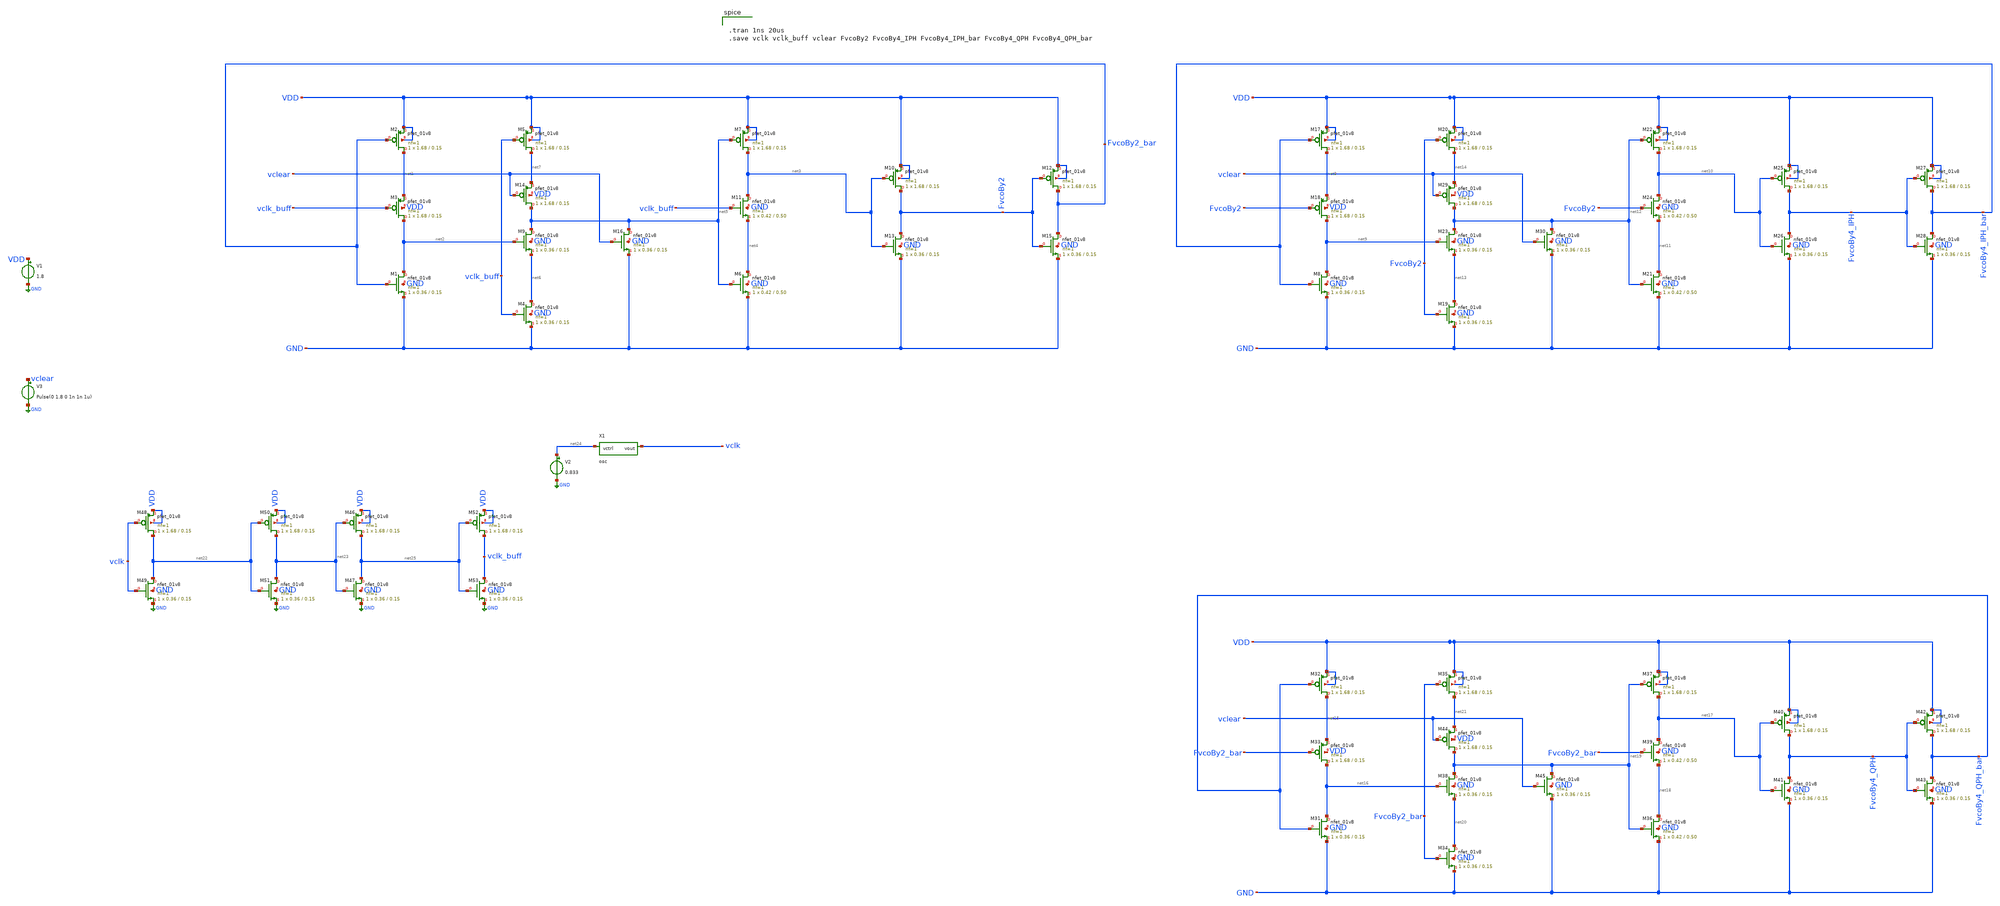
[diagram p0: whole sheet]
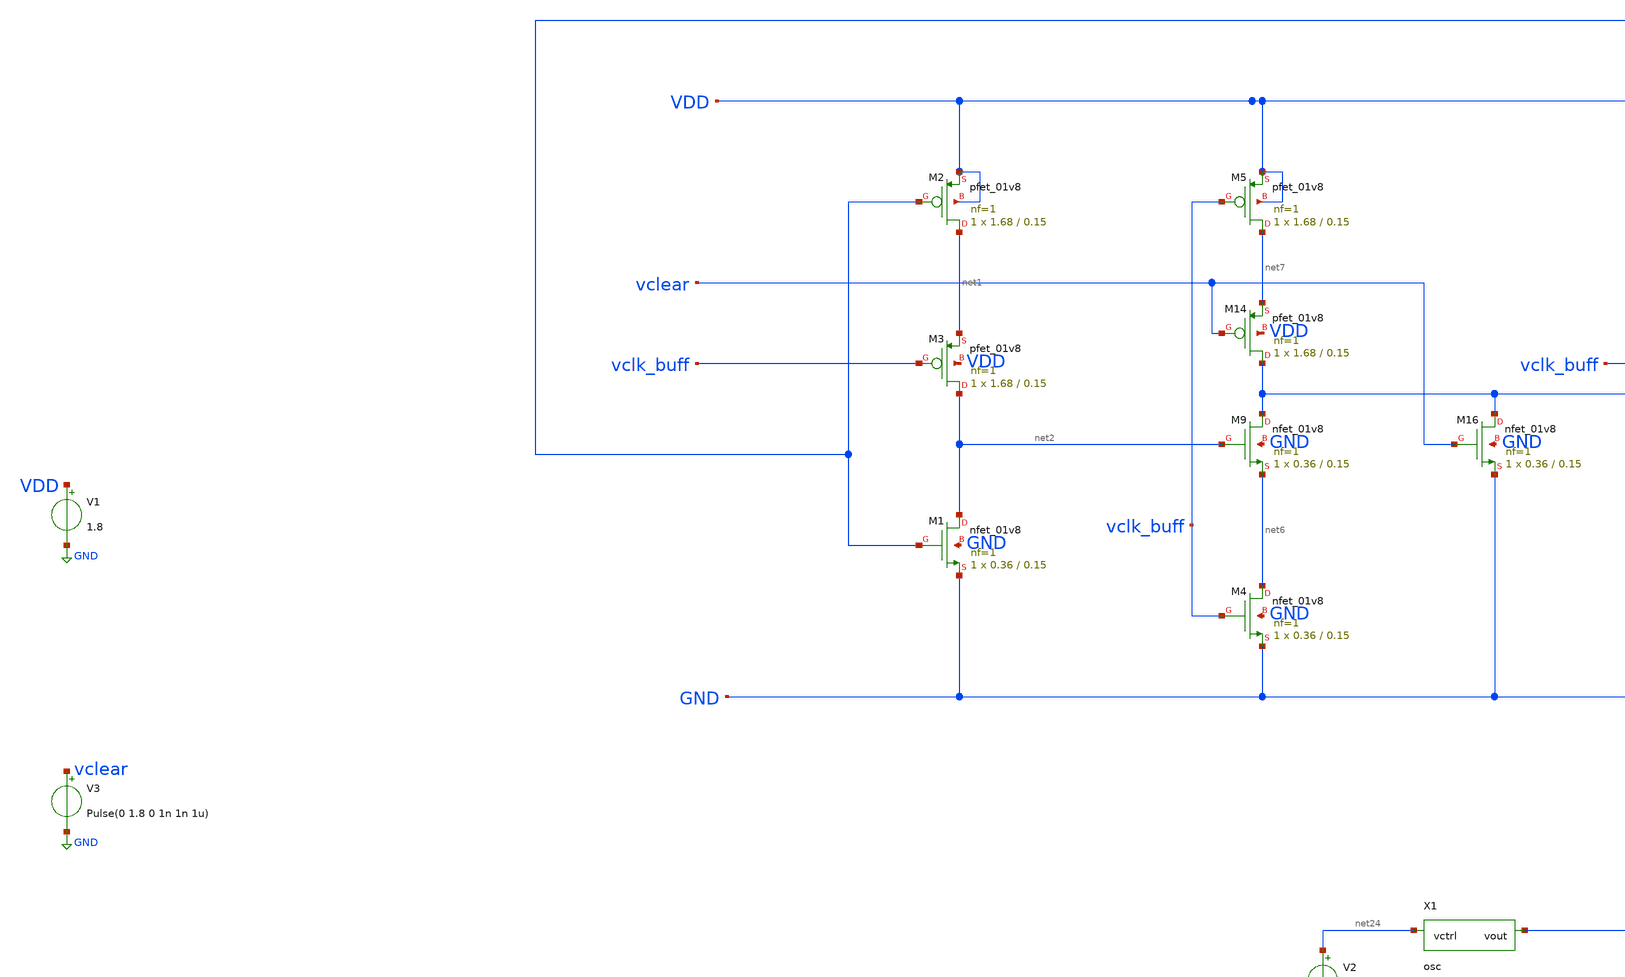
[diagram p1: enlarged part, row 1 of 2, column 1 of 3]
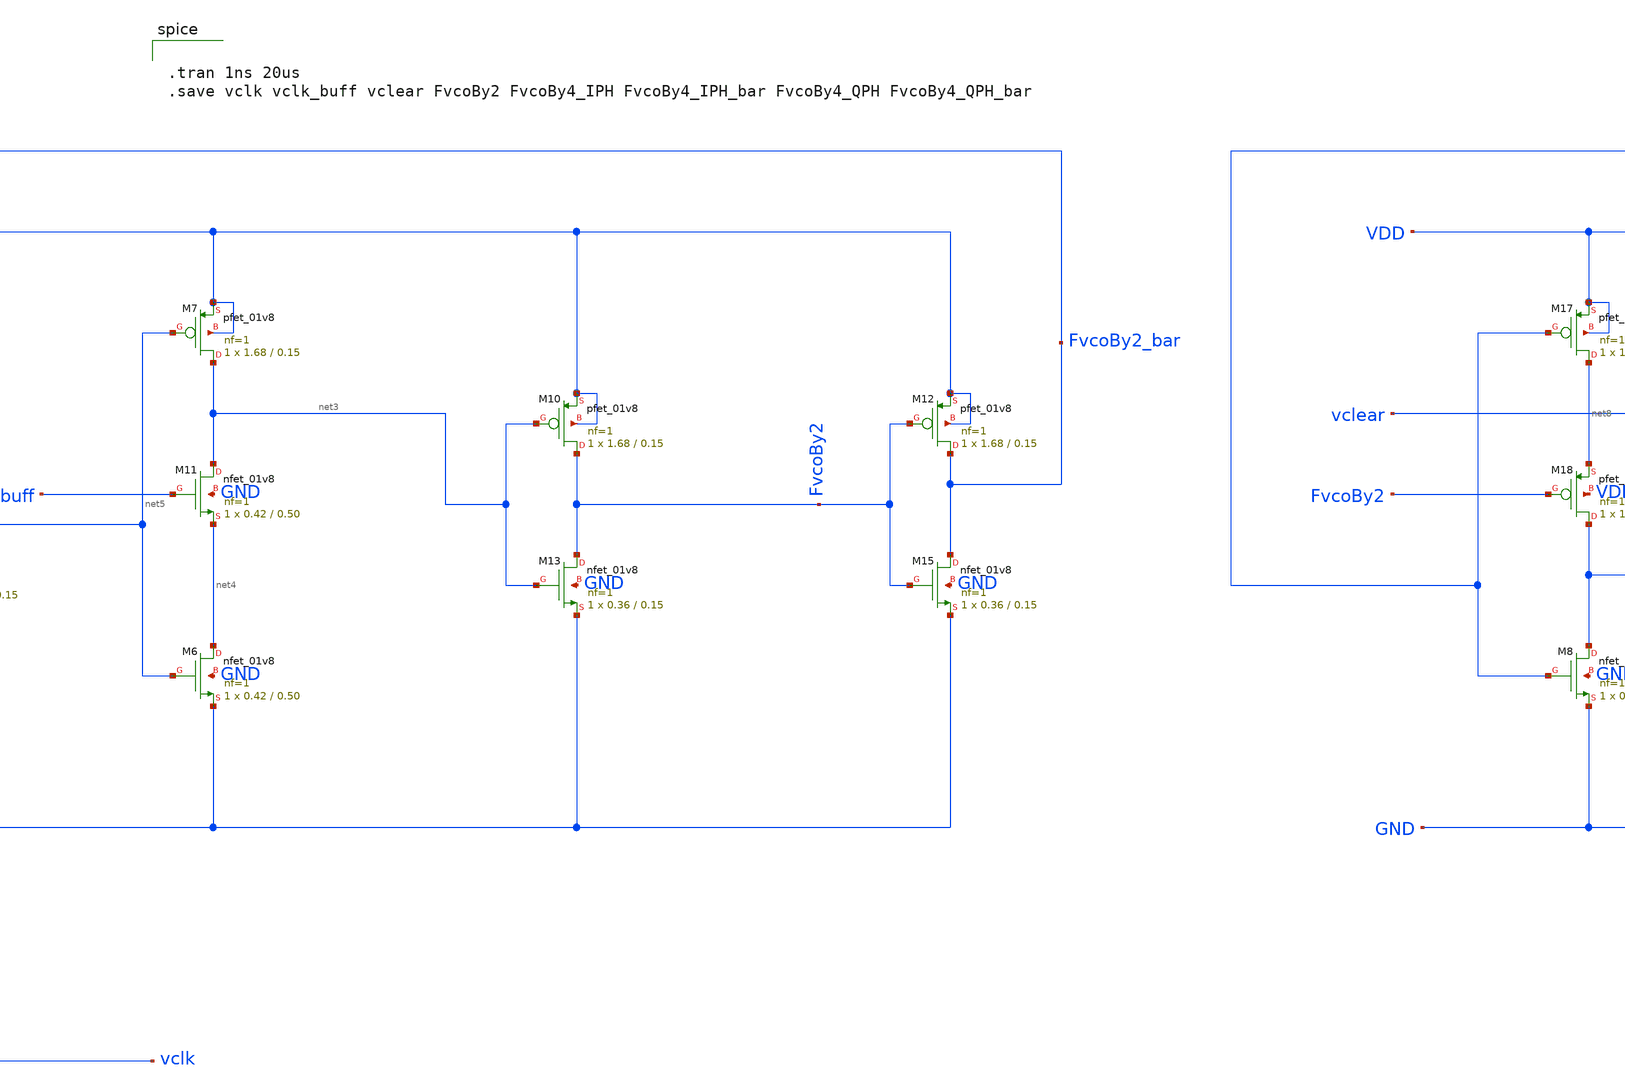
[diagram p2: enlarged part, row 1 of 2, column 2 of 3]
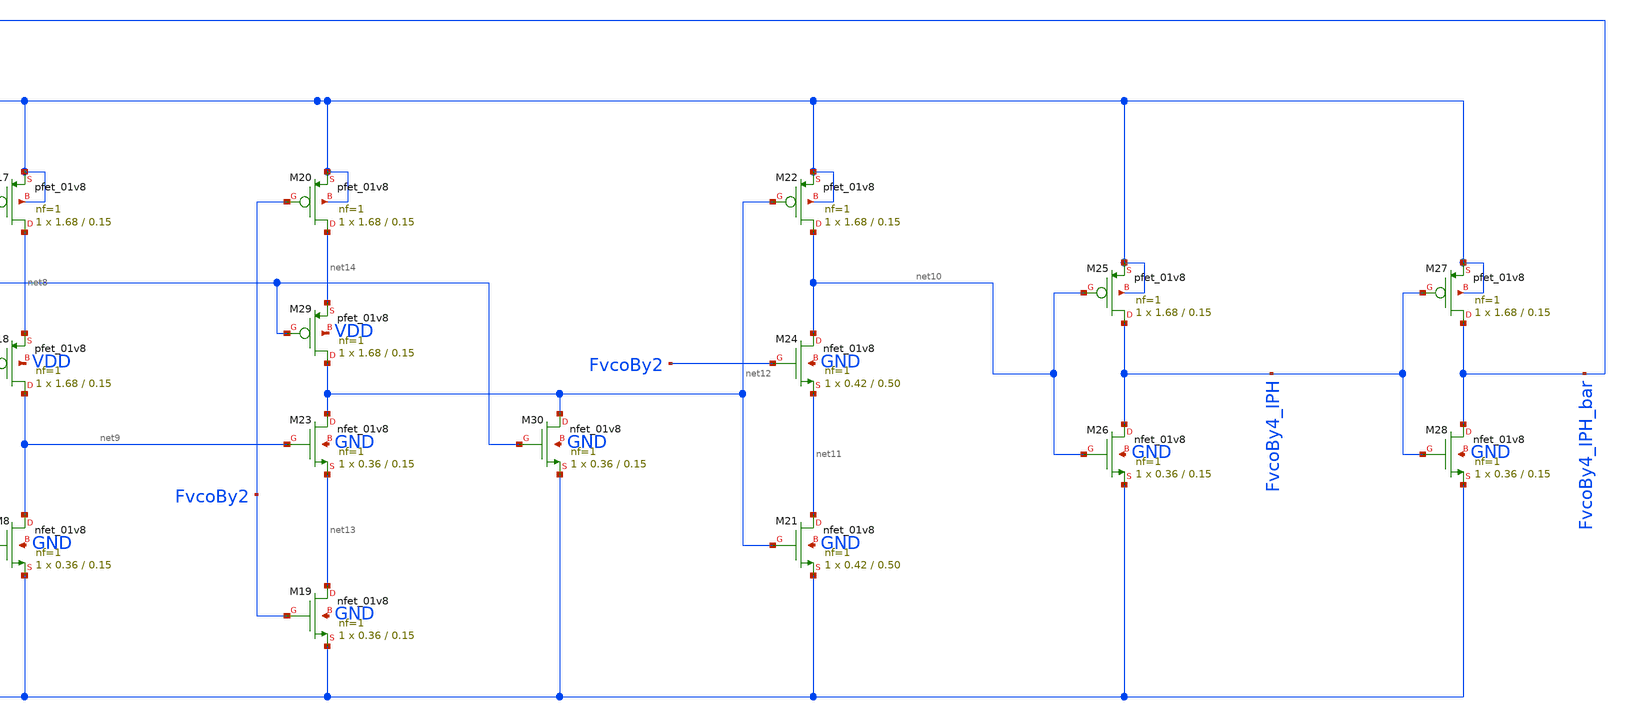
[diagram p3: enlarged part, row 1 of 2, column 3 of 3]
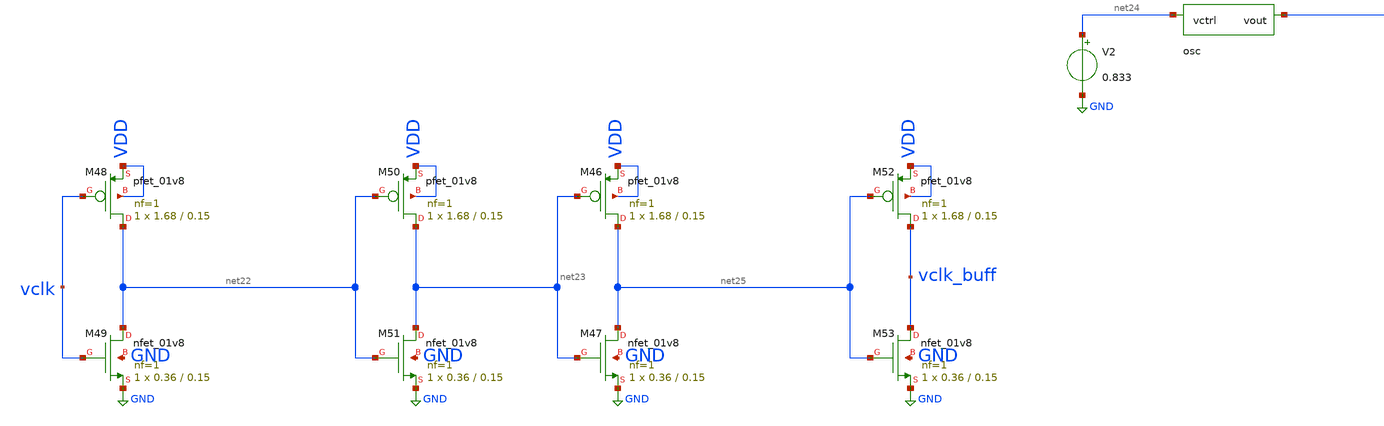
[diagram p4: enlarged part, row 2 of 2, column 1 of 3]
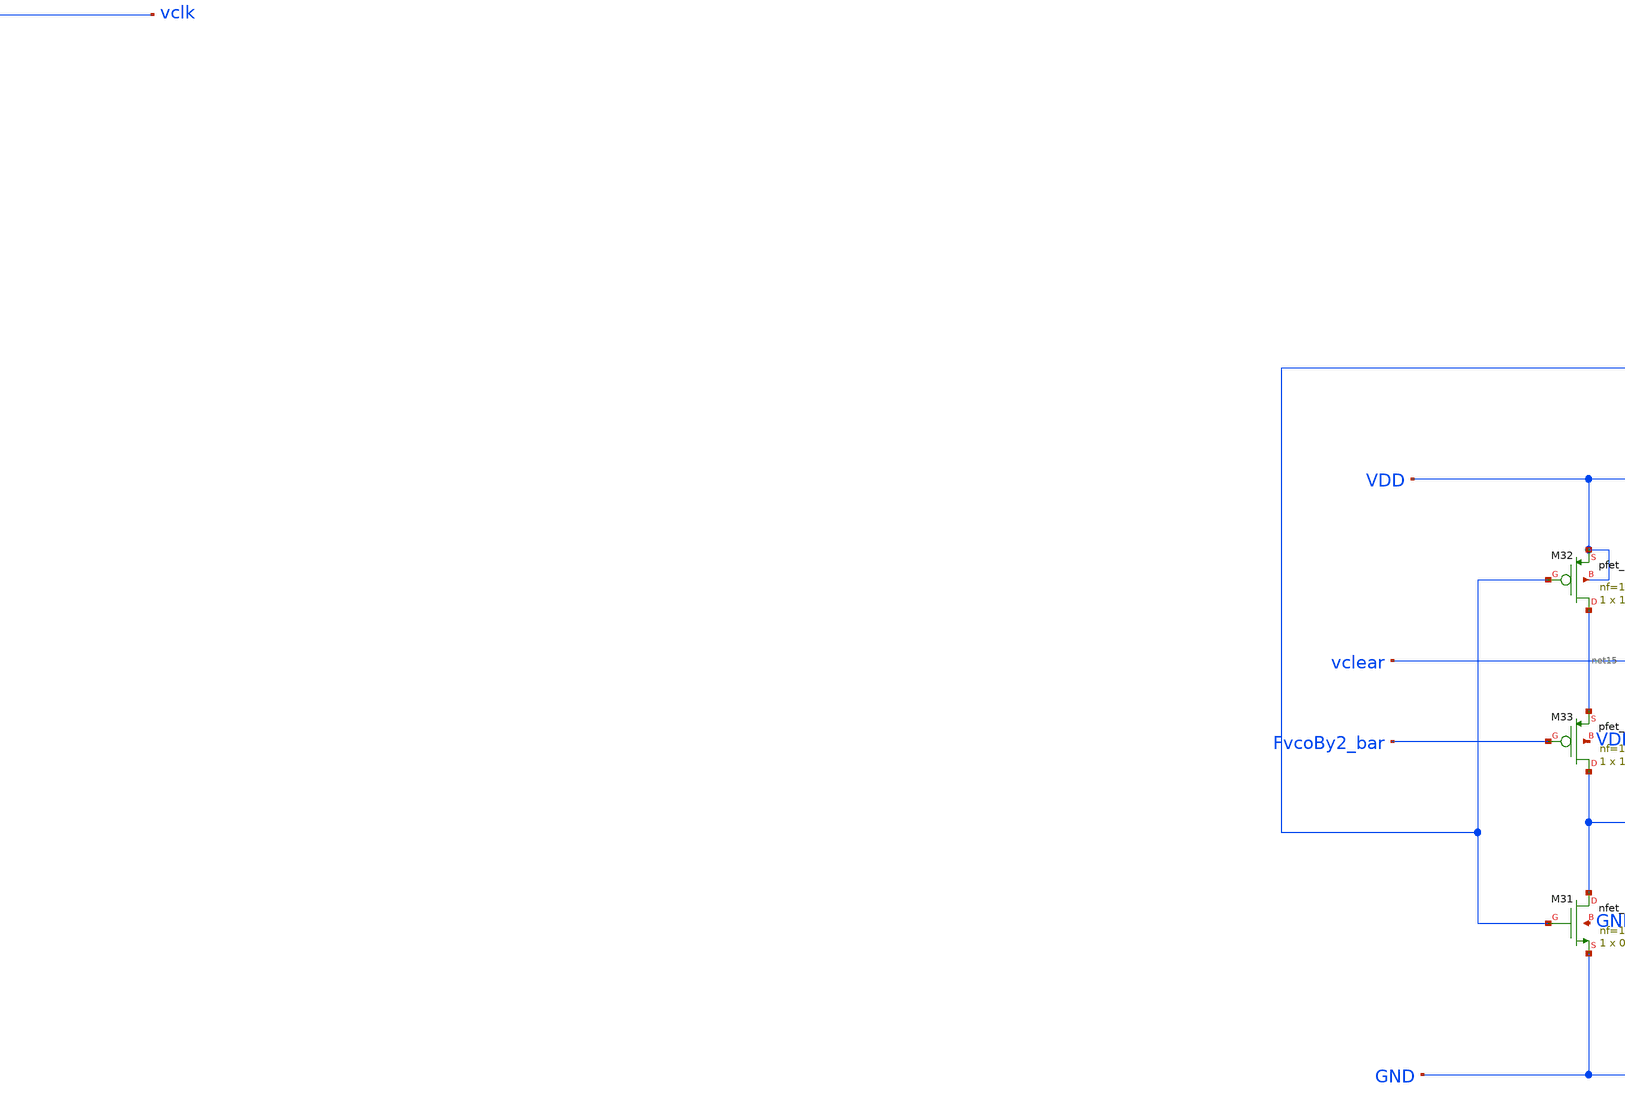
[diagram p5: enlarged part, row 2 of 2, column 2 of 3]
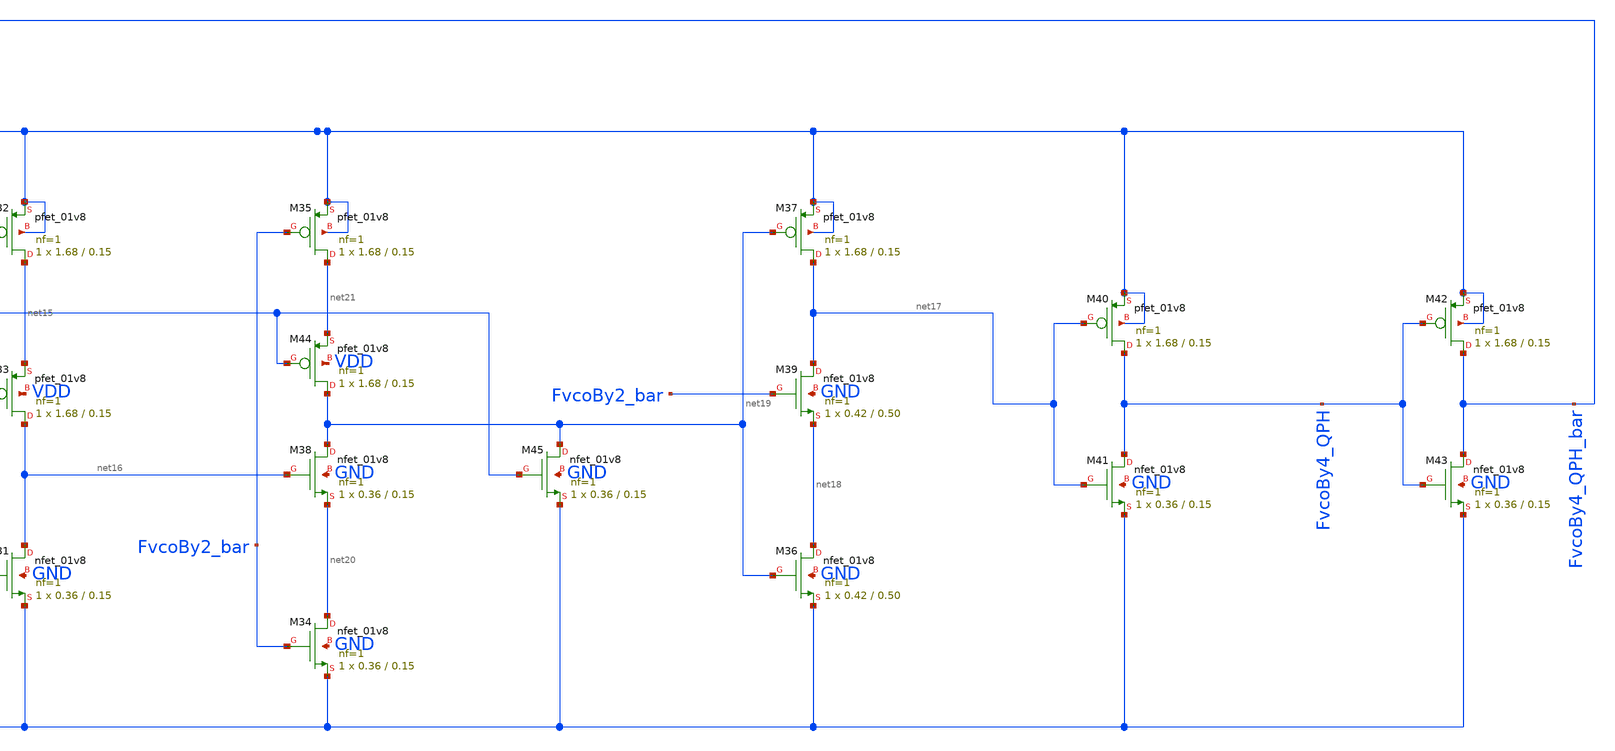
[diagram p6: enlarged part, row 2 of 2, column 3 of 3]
** sch_path: freqBy4_instant.sch
**.subckt freqBy4_instant
XM1 net2 FvcoBy2_bar GND GND sky130_fd_pr__nfet_01v8 L=0.15 W=0.36 nf=1 ad='int((nf+1)/2) * W/nf * 0.29'
+ as='int((nf+2)/2) * W/nf * 0.29' pd='2*int((nf+1)/2) * (W/nf + 0.29)' ps='2*int((nf+2)/2) * (W/nf + 0.29)'
+ nrd='0.29 / W' nrs='0.29 / W' sa=0 sb=0 sd=0 mult=1 m=1
XM2 net1 FvcoBy2_bar VDD VDD sky130_fd_pr__pfet_01v8 L=0.15 W=1.68 nf=1 ad='int((nf+1)/2) * W/nf * 0.29'
+ as='int((nf+2)/2) * W/nf * 0.29' pd='2*int((nf+1)/2) * (W/nf + 0.29)' ps='2*int((nf+2)/2) * (W/nf + 0.29)'
+ nrd='0.29 / W' nrs='0.29 / W' sa=0 sb=0 sd=0 mult=1 m=1
XM3 net2 vclk_buff net1 VDD sky130_fd_pr__pfet_01v8 L=0.15 W=1.68 nf=1 ad='int((nf+1)/2) * W/nf * 0.29'
+ as='int((nf+2)/2) * W/nf * 0.29' pd='2*int((nf+1)/2) * (W/nf + 0.29)' ps='2*int((nf+2)/2) * (W/nf + 0.29)'
+ nrd='0.29 / W' nrs='0.29 / W' sa=0 sb=0 sd=0 mult=1 m=1
XM4 net6 vclk_buff GND GND sky130_fd_pr__nfet_01v8 L=0.15 W=0.36 nf=1 ad='int((nf+1)/2) * W/nf * 0.29'
+ as='int((nf+2)/2) * W/nf * 0.29' pd='2*int((nf+1)/2) * (W/nf + 0.29)' ps='2*int((nf+2)/2) * (W/nf + 0.29)'
+ nrd='0.29 / W' nrs='0.29 / W' sa=0 sb=0 sd=0 mult=1 m=1
XM5 net7 vclk_buff VDD VDD sky130_fd_pr__pfet_01v8 L=0.15 W=1.68 nf=1 ad='int((nf+1)/2) * W/nf * 0.29'
+ as='int((nf+2)/2) * W/nf * 0.29' pd='2*int((nf+1)/2) * (W/nf + 0.29)' ps='2*int((nf+2)/2) * (W/nf + 0.29)'
+ nrd='0.29 / W' nrs='0.29 / W' sa=0 sb=0 sd=0 mult=1 m=1
XM6 net4 net5 GND GND sky130_fd_pr__nfet_01v8 L=0.50 W=0.42 nf=1 ad='int((nf+1)/2) * W/nf * 0.29' as='int((nf+2)/2) * W/nf * 0.29'
+ pd='2*int((nf+1)/2) * (W/nf + 0.29)' ps='2*int((nf+2)/2) * (W/nf + 0.29)' nrd='0.29 / W' nrs='0.29 / W'
+ sa=0 sb=0 sd=0 mult=1 m=1
XM7 net3 net5 VDD VDD sky130_fd_pr__pfet_01v8 L=0.15 W=1.68 nf=1 ad='int((nf+1)/2) * W/nf * 0.29' as='int((nf+2)/2) * W/nf * 0.29'
+ pd='2*int((nf+1)/2) * (W/nf + 0.29)' ps='2*int((nf+2)/2) * (W/nf + 0.29)' nrd='0.29 / W' nrs='0.29 / W'
+ sa=0 sb=0 sd=0 mult=1 m=1
XM9 net5 net2 net6 GND sky130_fd_pr__nfet_01v8 L=0.15 W=0.36 nf=1 ad='int((nf+1)/2) * W/nf * 0.29' as='int((nf+2)/2) * W/nf * 0.29'
+ pd='2*int((nf+1)/2) * (W/nf + 0.29)' ps='2*int((nf+2)/2) * (W/nf + 0.29)' nrd='0.29 / W' nrs='0.29 / W'
+ sa=0 sb=0 sd=0 mult=1 m=1
XM11 net3 vclk_buff net4 GND sky130_fd_pr__nfet_01v8 L=0.50 W=0.42 nf=1 ad='int((nf+1)/2) * W/nf * 0.29'
+ as='int((nf+2)/2) * W/nf * 0.29' pd='2*int((nf+1)/2) * (W/nf + 0.29)' ps='2*int((nf+2)/2) * (W/nf + 0.29)'
+ nrd='0.29 / W' nrs='0.29 / W' sa=0 sb=0 sd=0 mult=1 m=1
XM10 FvcoBy2 net3 VDD VDD sky130_fd_pr__pfet_01v8 L=0.15 W=1.68 nf=1 ad='int((nf+1)/2) * W/nf * 0.29'
+ as='int((nf+2)/2) * W/nf * 0.29' pd='2*int((nf+1)/2) * (W/nf + 0.29)' ps='2*int((nf+2)/2) * (W/nf + 0.29)'
+ nrd='0.29 / W' nrs='0.29 / W' sa=0 sb=0 sd=0 mult=1 m=1
XM13 FvcoBy2 net3 GND GND sky130_fd_pr__nfet_01v8 L=0.15 W=0.36 nf=1 ad='int((nf+1)/2) * W/nf * 0.29'
+ as='int((nf+2)/2) * W/nf * 0.29' pd='2*int((nf+1)/2) * (W/nf + 0.29)' ps='2*int((nf+2)/2) * (W/nf + 0.29)'
+ nrd='0.29 / W' nrs='0.29 / W' sa=0 sb=0 sd=0 mult=1 m=1
XM12 FvcoBy2_bar FvcoBy2 VDD VDD sky130_fd_pr__pfet_01v8 L=0.15 W=1.68 nf=1 ad='int((nf+1)/2) * W/nf * 0.29'
+ as='int((nf+2)/2) * W/nf * 0.29' pd='2*int((nf+1)/2) * (W/nf + 0.29)' ps='2*int((nf+2)/2) * (W/nf + 0.29)'
+ nrd='0.29 / W' nrs='0.29 / W' sa=0 sb=0 sd=0 mult=1 m=1
XM15 FvcoBy2_bar FvcoBy2 GND GND sky130_fd_pr__nfet_01v8 L=0.15 W=0.36 nf=1 ad='int((nf+1)/2) * W/nf * 0.29'
+ as='int((nf+2)/2) * W/nf * 0.29' pd='2*int((nf+1)/2) * (W/nf + 0.29)' ps='2*int((nf+2)/2) * (W/nf + 0.29)'
+ nrd='0.29 / W' nrs='0.29 / W' sa=0 sb=0 sd=0 mult=1 m=1
XM14 net5 vclear net7 VDD sky130_fd_pr__pfet_01v8 L=0.15 W=1.68 nf=1 ad='int((nf+1)/2) * W/nf * 0.29'
+ as='int((nf+2)/2) * W/nf * 0.29' pd='2*int((nf+1)/2) * (W/nf + 0.29)' ps='2*int((nf+2)/2) * (W/nf + 0.29)'
+ nrd='0.29 / W' nrs='0.29 / W' sa=0 sb=0 sd=0 mult=1 m=1
XM16 net5 vclear GND GND sky130_fd_pr__nfet_01v8 L=0.15 W=0.36 nf=1 ad='int((nf+1)/2) * W/nf * 0.29'
+ as='int((nf+2)/2) * W/nf * 0.29' pd='2*int((nf+1)/2) * (W/nf + 0.29)' ps='2*int((nf+2)/2) * (W/nf + 0.29)'
+ nrd='0.29 / W' nrs='0.29 / W' sa=0 sb=0 sd=0 mult=1 m=1
XM8 net9 FvcoBy4_IPH_bar GND GND sky130_fd_pr__nfet_01v8 L=0.15 W=0.36 nf=1 ad='int((nf+1)/2) * W/nf * 0.29'
+ as='int((nf+2)/2) * W/nf * 0.29' pd='2*int((nf+1)/2) * (W/nf + 0.29)' ps='2*int((nf+2)/2) * (W/nf + 0.29)'
+ nrd='0.29 / W' nrs='0.29 / W' sa=0 sb=0 sd=0 mult=1 m=1
XM17 net8 FvcoBy4_IPH_bar VDD VDD sky130_fd_pr__pfet_01v8 L=0.15 W=1.68 nf=1 ad='int((nf+1)/2) * W/nf * 0.29'
+ as='int((nf+2)/2) * W/nf * 0.29' pd='2*int((nf+1)/2) * (W/nf + 0.29)' ps='2*int((nf+2)/2) * (W/nf + 0.29)'
+ nrd='0.29 / W' nrs='0.29 / W' sa=0 sb=0 sd=0 mult=1 m=1
XM18 net9 FvcoBy2 net8 VDD sky130_fd_pr__pfet_01v8 L=0.15 W=1.68 nf=1 ad='int((nf+1)/2) * W/nf * 0.29'
+ as='int((nf+2)/2) * W/nf * 0.29' pd='2*int((nf+1)/2) * (W/nf + 0.29)' ps='2*int((nf+2)/2) * (W/nf + 0.29)'
+ nrd='0.29 / W' nrs='0.29 / W' sa=0 sb=0 sd=0 mult=1 m=1
XM19 net13 FvcoBy2 GND GND sky130_fd_pr__nfet_01v8 L=0.15 W=0.36 nf=1 ad='int((nf+1)/2) * W/nf * 0.29'
+ as='int((nf+2)/2) * W/nf * 0.29' pd='2*int((nf+1)/2) * (W/nf + 0.29)' ps='2*int((nf+2)/2) * (W/nf + 0.29)'
+ nrd='0.29 / W' nrs='0.29 / W' sa=0 sb=0 sd=0 mult=1 m=1
XM20 net14 FvcoBy2 VDD VDD sky130_fd_pr__pfet_01v8 L=0.15 W=1.68 nf=1 ad='int((nf+1)/2) * W/nf * 0.29'
+ as='int((nf+2)/2) * W/nf * 0.29' pd='2*int((nf+1)/2) * (W/nf + 0.29)' ps='2*int((nf+2)/2) * (W/nf + 0.29)'
+ nrd='0.29 / W' nrs='0.29 / W' sa=0 sb=0 sd=0 mult=1 m=1
XM21 net11 net12 GND GND sky130_fd_pr__nfet_01v8 L=0.50 W=0.42 nf=1 ad='int((nf+1)/2) * W/nf * 0.29'
+ as='int((nf+2)/2) * W/nf * 0.29' pd='2*int((nf+1)/2) * (W/nf + 0.29)' ps='2*int((nf+2)/2) * (W/nf + 0.29)'
+ nrd='0.29 / W' nrs='0.29 / W' sa=0 sb=0 sd=0 mult=1 m=1
XM22 net10 net12 VDD VDD sky130_fd_pr__pfet_01v8 L=0.15 W=1.68 nf=1 ad='int((nf+1)/2) * W/nf * 0.29'
+ as='int((nf+2)/2) * W/nf * 0.29' pd='2*int((nf+1)/2) * (W/nf + 0.29)' ps='2*int((nf+2)/2) * (W/nf + 0.29)'
+ nrd='0.29 / W' nrs='0.29 / W' sa=0 sb=0 sd=0 mult=1 m=1
XM23 net12 net9 net13 GND sky130_fd_pr__nfet_01v8 L=0.15 W=0.36 nf=1 ad='int((nf+1)/2) * W/nf * 0.29'
+ as='int((nf+2)/2) * W/nf * 0.29' pd='2*int((nf+1)/2) * (W/nf + 0.29)' ps='2*int((nf+2)/2) * (W/nf + 0.29)'
+ nrd='0.29 / W' nrs='0.29 / W' sa=0 sb=0 sd=0 mult=1 m=1
XM24 net10 FvcoBy2 net11 GND sky130_fd_pr__nfet_01v8 L=0.50 W=0.42 nf=1 ad='int((nf+1)/2) * W/nf * 0.29'
+ as='int((nf+2)/2) * W/nf * 0.29' pd='2*int((nf+1)/2) * (W/nf + 0.29)' ps='2*int((nf+2)/2) * (W/nf + 0.29)'
+ nrd='0.29 / W' nrs='0.29 / W' sa=0 sb=0 sd=0 mult=1 m=1
XM25 FvcoBy4_IPH net10 VDD VDD sky130_fd_pr__pfet_01v8 L=0.15 W=1.68 nf=1 ad='int((nf+1)/2) * W/nf * 0.29'
+ as='int((nf+2)/2) * W/nf * 0.29' pd='2*int((nf+1)/2) * (W/nf + 0.29)' ps='2*int((nf+2)/2) * (W/nf + 0.29)'
+ nrd='0.29 / W' nrs='0.29 / W' sa=0 sb=0 sd=0 mult=1 m=1
XM26 FvcoBy4_IPH net10 GND GND sky130_fd_pr__nfet_01v8 L=0.15 W=0.36 nf=1 ad='int((nf+1)/2) * W/nf * 0.29'
+ as='int((nf+2)/2) * W/nf * 0.29' pd='2*int((nf+1)/2) * (W/nf + 0.29)' ps='2*int((nf+2)/2) * (W/nf + 0.29)'
+ nrd='0.29 / W' nrs='0.29 / W' sa=0 sb=0 sd=0 mult=1 m=1
XM27 FvcoBy4_IPH_bar FvcoBy4_IPH VDD VDD sky130_fd_pr__pfet_01v8 L=0.15 W=1.68 nf=1 ad='int((nf+1)/2) * W/nf * 0.29'
+ as='int((nf+2)/2) * W/nf * 0.29' pd='2*int((nf+1)/2) * (W/nf + 0.29)' ps='2*int((nf+2)/2) * (W/nf + 0.29)'
+ nrd='0.29 / W' nrs='0.29 / W' sa=0 sb=0 sd=0 mult=1 m=1
XM28 FvcoBy4_IPH_bar FvcoBy4_IPH GND GND sky130_fd_pr__nfet_01v8 L=0.15 W=0.36 nf=1 ad='int((nf+1)/2) * W/nf * 0.29'
+ as='int((nf+2)/2) * W/nf * 0.29' pd='2*int((nf+1)/2) * (W/nf + 0.29)' ps='2*int((nf+2)/2) * (W/nf + 0.29)'
+ nrd='0.29 / W' nrs='0.29 / W' sa=0 sb=0 sd=0 mult=1 m=1
XM29 net12 vclear net14 VDD sky130_fd_pr__pfet_01v8 L=0.15 W=1.68 nf=1 ad='int((nf+1)/2) * W/nf * 0.29'
+ as='int((nf+2)/2) * W/nf * 0.29' pd='2*int((nf+1)/2) * (W/nf + 0.29)' ps='2*int((nf+2)/2) * (W/nf + 0.29)'
+ nrd='0.29 / W' nrs='0.29 / W' sa=0 sb=0 sd=0 mult=1 m=1
XM30 net12 vclear GND GND sky130_fd_pr__nfet_01v8 L=0.15 W=0.36 nf=1 ad='int((nf+1)/2) * W/nf * 0.29'
+ as='int((nf+2)/2) * W/nf * 0.29' pd='2*int((nf+1)/2) * (W/nf + 0.29)' ps='2*int((nf+2)/2) * (W/nf + 0.29)'
+ nrd='0.29 / W' nrs='0.29 / W' sa=0 sb=0 sd=0 mult=1 m=1
XM31 net16 FvcoBy4_QPH_bar GND GND sky130_fd_pr__nfet_01v8 L=0.15 W=0.36 nf=1 ad='int((nf+1)/2) * W/nf * 0.29'
+ as='int((nf+2)/2) * W/nf * 0.29' pd='2*int((nf+1)/2) * (W/nf + 0.29)' ps='2*int((nf+2)/2) * (W/nf + 0.29)'
+ nrd='0.29 / W' nrs='0.29 / W' sa=0 sb=0 sd=0 mult=1 m=1
XM32 net15 FvcoBy4_QPH_bar VDD VDD sky130_fd_pr__pfet_01v8 L=0.15 W=1.68 nf=1 ad='int((nf+1)/2) * W/nf * 0.29'
+ as='int((nf+2)/2) * W/nf * 0.29' pd='2*int((nf+1)/2) * (W/nf + 0.29)' ps='2*int((nf+2)/2) * (W/nf + 0.29)'
+ nrd='0.29 / W' nrs='0.29 / W' sa=0 sb=0 sd=0 mult=1 m=1
XM33 net16 FvcoBy2_bar net15 VDD sky130_fd_pr__pfet_01v8 L=0.15 W=1.68 nf=1 ad='int((nf+1)/2) * W/nf * 0.29'
+ as='int((nf+2)/2) * W/nf * 0.29' pd='2*int((nf+1)/2) * (W/nf + 0.29)' ps='2*int((nf+2)/2) * (W/nf + 0.29)'
+ nrd='0.29 / W' nrs='0.29 / W' sa=0 sb=0 sd=0 mult=1 m=1
XM34 net20 FvcoBy2_bar GND GND sky130_fd_pr__nfet_01v8 L=0.15 W=0.36 nf=1 ad='int((nf+1)/2) * W/nf * 0.29'
+ as='int((nf+2)/2) * W/nf * 0.29' pd='2*int((nf+1)/2) * (W/nf + 0.29)' ps='2*int((nf+2)/2) * (W/nf + 0.29)'
+ nrd='0.29 / W' nrs='0.29 / W' sa=0 sb=0 sd=0 mult=1 m=1
XM35 net21 FvcoBy2_bar VDD VDD sky130_fd_pr__pfet_01v8 L=0.15 W=1.68 nf=1 ad='int((nf+1)/2) * W/nf * 0.29'
+ as='int((nf+2)/2) * W/nf * 0.29' pd='2*int((nf+1)/2) * (W/nf + 0.29)' ps='2*int((nf+2)/2) * (W/nf + 0.29)'
+ nrd='0.29 / W' nrs='0.29 / W' sa=0 sb=0 sd=0 mult=1 m=1
XM36 net18 net19 GND GND sky130_fd_pr__nfet_01v8 L=0.50 W=0.42 nf=1 ad='int((nf+1)/2) * W/nf * 0.29'
+ as='int((nf+2)/2) * W/nf * 0.29' pd='2*int((nf+1)/2) * (W/nf + 0.29)' ps='2*int((nf+2)/2) * (W/nf + 0.29)'
+ nrd='0.29 / W' nrs='0.29 / W' sa=0 sb=0 sd=0 mult=1 m=1
XM37 net17 net19 VDD VDD sky130_fd_pr__pfet_01v8 L=0.15 W=1.68 nf=1 ad='int((nf+1)/2) * W/nf * 0.29'
+ as='int((nf+2)/2) * W/nf * 0.29' pd='2*int((nf+1)/2) * (W/nf + 0.29)' ps='2*int((nf+2)/2) * (W/nf + 0.29)'
+ nrd='0.29 / W' nrs='0.29 / W' sa=0 sb=0 sd=0 mult=1 m=1
XM38 net19 net16 net20 GND sky130_fd_pr__nfet_01v8 L=0.15 W=0.36 nf=1 ad='int((nf+1)/2) * W/nf * 0.29'
+ as='int((nf+2)/2) * W/nf * 0.29' pd='2*int((nf+1)/2) * (W/nf + 0.29)' ps='2*int((nf+2)/2) * (W/nf + 0.29)'
+ nrd='0.29 / W' nrs='0.29 / W' sa=0 sb=0 sd=0 mult=1 m=1
XM39 net17 FvcoBy2_bar net18 GND sky130_fd_pr__nfet_01v8 L=0.50 W=0.42 nf=1 ad='int((nf+1)/2) * W/nf * 0.29'
+ as='int((nf+2)/2) * W/nf * 0.29' pd='2*int((nf+1)/2) * (W/nf + 0.29)' ps='2*int((nf+2)/2) * (W/nf + 0.29)'
+ nrd='0.29 / W' nrs='0.29 / W' sa=0 sb=0 sd=0 mult=1 m=1
XM40 FvcoBy4_QPH net17 VDD VDD sky130_fd_pr__pfet_01v8 L=0.15 W=1.68 nf=1 ad='int((nf+1)/2) * W/nf * 0.29'
+ as='int((nf+2)/2) * W/nf * 0.29' pd='2*int((nf+1)/2) * (W/nf + 0.29)' ps='2*int((nf+2)/2) * (W/nf + 0.29)'
+ nrd='0.29 / W' nrs='0.29 / W' sa=0 sb=0 sd=0 mult=1 m=1
XM41 FvcoBy4_QPH net17 GND GND sky130_fd_pr__nfet_01v8 L=0.15 W=0.36 nf=1 ad='int((nf+1)/2) * W/nf * 0.29'
+ as='int((nf+2)/2) * W/nf * 0.29' pd='2*int((nf+1)/2) * (W/nf + 0.29)' ps='2*int((nf+2)/2) * (W/nf + 0.29)'
+ nrd='0.29 / W' nrs='0.29 / W' sa=0 sb=0 sd=0 mult=1 m=1
XM42 FvcoBy4_QPH_bar FvcoBy4_QPH VDD VDD sky130_fd_pr__pfet_01v8 L=0.15 W=1.68 nf=1 ad='int((nf+1)/2) * W/nf * 0.29'
+ as='int((nf+2)/2) * W/nf * 0.29' pd='2*int((nf+1)/2) * (W/nf + 0.29)' ps='2*int((nf+2)/2) * (W/nf + 0.29)'
+ nrd='0.29 / W' nrs='0.29 / W' sa=0 sb=0 sd=0 mult=1 m=1
XM43 FvcoBy4_QPH_bar FvcoBy4_QPH GND GND sky130_fd_pr__nfet_01v8 L=0.15 W=0.36 nf=1 ad='int((nf+1)/2) * W/nf * 0.29'
+ as='int((nf+2)/2) * W/nf * 0.29' pd='2*int((nf+1)/2) * (W/nf + 0.29)' ps='2*int((nf+2)/2) * (W/nf + 0.29)'
+ nrd='0.29 / W' nrs='0.29 / W' sa=0 sb=0 sd=0 mult=1 m=1
XM44 net19 vclear net21 VDD sky130_fd_pr__pfet_01v8 L=0.15 W=1.68 nf=1 ad='int((nf+1)/2) * W/nf * 0.29'
+ as='int((nf+2)/2) * W/nf * 0.29' pd='2*int((nf+1)/2) * (W/nf + 0.29)' ps='2*int((nf+2)/2) * (W/nf + 0.29)'
+ nrd='0.29 / W' nrs='0.29 / W' sa=0 sb=0 sd=0 mult=1 m=1
XM45 net19 vclear GND GND sky130_fd_pr__nfet_01v8 L=0.15 W=0.36 nf=1 ad='int((nf+1)/2) * W/nf * 0.29'
+ as='int((nf+2)/2) * W/nf * 0.29' pd='2*int((nf+1)/2) * (W/nf + 0.29)' ps='2*int((nf+2)/2) * (W/nf + 0.29)'
+ nrd='0.29 / W' nrs='0.29 / W' sa=0 sb=0 sd=0 mult=1 m=1
V1 VDD GND 1.8
V3 vclear GND Pulse(0 1.8 0 1n 1n 1u)
XM48 net22 vclk VDD VDD sky130_fd_pr__pfet_01v8 L=0.15 W=1.68 nf=1 ad='int((nf+1)/2) * W/nf * 0.29' as='int((nf+2)/2) * W/nf * 0.29'
+ pd='2*int((nf+1)/2) * (W/nf + 0.29)' ps='2*int((nf+2)/2) * (W/nf + 0.29)' nrd='0.29 / W' nrs='0.29 / W'
+ sa=0 sb=0 sd=0 mult=1 m=1
XM49 net22 vclk GND GND sky130_fd_pr__nfet_01v8 L=0.15 W=0.36 nf=1 ad='int((nf+1)/2) * W/nf * 0.29' as='int((nf+2)/2) * W/nf * 0.29'
+ pd='2*int((nf+1)/2) * (W/nf + 0.29)' ps='2*int((nf+2)/2) * (W/nf + 0.29)' nrd='0.29 / W' nrs='0.29 / W'
+ sa=0 sb=0 sd=0 mult=1 m=1
XM50 net23 net22 VDD VDD sky130_fd_pr__pfet_01v8 L=0.15 W=1.68 nf=1 ad='int((nf+1)/2) * W/nf * 0.29'
+ as='int((nf+2)/2) * W/nf * 0.29' pd='2*int((nf+1)/2) * (W/nf + 0.29)' ps='2*int((nf+2)/2) * (W/nf + 0.29)'
+ nrd='0.29 / W' nrs='0.29 / W' sa=0 sb=0 sd=0 mult=1 m=1
XM51 net23 net22 GND GND sky130_fd_pr__nfet_01v8 L=0.15 W=0.36 nf=1 ad='int((nf+1)/2) * W/nf * 0.29'
+ as='int((nf+2)/2) * W/nf * 0.29' pd='2*int((nf+1)/2) * (W/nf + 0.29)' ps='2*int((nf+2)/2) * (W/nf + 0.29)'
+ nrd='0.29 / W' nrs='0.29 / W' sa=0 sb=0 sd=0 mult=1 m=1
V2 net24 GND 0.833
XM46 net25 net23 VDD VDD sky130_fd_pr__pfet_01v8 L=0.15 W=1.68 nf=1 ad='int((nf+1)/2) * W/nf * 0.29'
+ as='int((nf+2)/2) * W/nf * 0.29' pd='2*int((nf+1)/2) * (W/nf + 0.29)' ps='2*int((nf+2)/2) * (W/nf + 0.29)'
+ nrd='0.29 / W' nrs='0.29 / W' sa=0 sb=0 sd=0 mult=1 m=1
XM47 net25 net23 GND GND sky130_fd_pr__nfet_01v8 L=0.15 W=0.36 nf=1 ad='int((nf+1)/2) * W/nf * 0.29'
+ as='int((nf+2)/2) * W/nf * 0.29' pd='2*int((nf+1)/2) * (W/nf + 0.29)' ps='2*int((nf+2)/2) * (W/nf + 0.29)'
+ nrd='0.29 / W' nrs='0.29 / W' sa=0 sb=0 sd=0 mult=1 m=1
XM52 vclk_buff net25 VDD VDD sky130_fd_pr__pfet_01v8 L=0.15 W=1.68 nf=1 ad='int((nf+1)/2) * W/nf * 0.29'
+ as='int((nf+2)/2) * W/nf * 0.29' pd='2*int((nf+1)/2) * (W/nf + 0.29)' ps='2*int((nf+2)/2) * (W/nf + 0.29)'
+ nrd='0.29 / W' nrs='0.29 / W' sa=0 sb=0 sd=0 mult=1 m=1
XM53 vclk_buff net25 GND GND sky130_fd_pr__nfet_01v8 L=0.15 W=0.36 nf=1 ad='int((nf+1)/2) * W/nf * 0.29'
+ as='int((nf+2)/2) * W/nf * 0.29' pd='2*int((nf+1)/2) * (W/nf + 0.29)' ps='2*int((nf+2)/2) * (W/nf + 0.29)'
+ nrd='0.29 / W' nrs='0.29 / W' sa=0 sb=0 sd=0 mult=1 m=1
X1 net24 vclk osc
**** begin user architecture code


.tran 1ns 20us
.save vclk vclk_buff vclear FvcoBy2 FvcoBy4_IPH FvcoBy4_IPH_bar FvcoBy4_QPH FvcoBy4_QPH_bar



*.lib ~/open_pdks/sky130/sky130A/libs.tech/ngspice/sky130.lib.spice tt
.param mc_mm_switch=0
.param mc_pr_switch=0

.include ~/open_pdks/sky130/sky130A/libs.tech/ngspice/corners/tt/nonfet.spice


*model
.include ~/open_pdks/sky130/sky130A/libs.tech/ngspice/all.spice

*mosfet
.include ~/open_pdks/sky130/sky130A/libs.ref/sky130_fd_pr/spice/sky130_fd_pr__pfet_01v8__tt.corner.spice
.inclued ~/open_pdks/sky130/sky130A/libs.ref/sky130_fd_pr/spice/sky130_fd_pr__nfet_01v8__tt.corner.spice

*mismatch parameters
.include ~/open_pdks/sky130/sky130A/libs.ref/sky130_fd_pr/spice/sky130_fd_pr__pfet_01v8__mismatch.corner.spice
.include ~/open_pdks/sky130/sky130A/libs.ref/sky130_fd_pr/spice/sky130_fd_pr__nfet_01v8__mismatch.corner.spice


*mosfet
.include ~/open_pdks/sky130/sky130A/libs.ref/sky130_fd_pr/spice/sky130_fd_pr__pfet_01v8_lvt__tt.corner.spice
.inclued ~/open_pdks/sky130/sky130A/libs.ref/sky130_fd_pr/spice/sky130_fd_pr__nfet_01v8_lvt__tt.corner.spice

*mismatch parameters
.include ~/open_pdks/sky130/sky130A/libs.ref/sky130_fd_pr/spice/sky130_fd_pr__pfet_01v8_lvt__mismatch.corner.spice
.include ~/open_pdks/sky130/sky130A/libs.ref/sky130_fd_pr/spice/sky130_fd_pr__nfet_01v8_lvt__mismatch.corner.spice

**** end user architecture code
**.ends

* expanding   symbol:  /home/cegrahul/Desktop/SSCS/osc.sym # of pins=2
** sym_path: osc.sym
** sch_path: osc.sch
.subckt osc vctrl vout
*.ipin vctrl
*.opin vout
XM1 net1 vout net2 GND sky130_fd_pr__nfet_01v8 L=4 W=0.55 nf=1 ad='int((nf+1)/2) * W/nf * 0.29' as='int((nf+2)/2) * W/nf * 0.29'
+ pd='2*int((nf+1)/2) * (W/nf + 0.29)' ps='2*int((nf+2)/2) * (W/nf + 0.29)' nrd='0.29 / W' nrs='0.29 / W'
+ sa=0 sb=0 sd=0 mult=1 m=1
XM3 net1 vout net3 net4 sky130_fd_pr__pfet_01v8 L=4 W=1 nf=1 ad='int((nf+1)/2) * W/nf * 0.29' as='int((nf+2)/2) * W/nf * 0.29'
+ pd='2*int((nf+1)/2) * (W/nf + 0.29)' ps='2*int((nf+2)/2) * (W/nf + 0.29)' nrd='0.29 / W' nrs='0.29 / W'
+ sa=0 sb=0 sd=0 mult=1 m=1
XM19 net2 vout GND GND sky130_fd_pr__nfet_01v8 L=4 W=0.55 nf=1 ad='int((nf+1)/2) * W/nf * 0.29' as='int((nf+2)/2) * W/nf * 0.29'
+ pd='2*int((nf+1)/2) * (W/nf + 0.29)' ps='2*int((nf+2)/2) * (W/nf + 0.29)' nrd='0.29 / W' nrs='0.29 / W'
+ sa=0 sb=0 sd=0 mult=1 m=1
XM29 net3 vctrl net4 net4 sky130_fd_pr__pfet_01v8 L=2 W=1 nf=1 ad='int((nf+1)/2) * W/nf * 0.29' as='int((nf+2)/2) * W/nf * 0.29'
+ pd='2*int((nf+1)/2) * (W/nf + 0.29)' ps='2*int((nf+2)/2) * (W/nf + 0.29)' nrd='0.29 / W' nrs='0.29 / W'
+ sa=0 sb=0 sd=0 mult=1 m=1
V3 net4 GND 1.8
XM2 net5 net1 net6 GND sky130_fd_pr__nfet_01v8 L=4 W=0.55 nf=1 ad='int((nf+1)/2) * W/nf * 0.29' as='int((nf+2)/2) * W/nf * 0.29'
+ pd='2*int((nf+1)/2) * (W/nf + 0.29)' ps='2*int((nf+2)/2) * (W/nf + 0.29)' nrd='0.29 / W' nrs='0.29 / W'
+ sa=0 sb=0 sd=0 mult=1 m=1
XM4 net5 net1 net3 net4 sky130_fd_pr__pfet_01v8 L=4 W=1 nf=1 ad='int((nf+1)/2) * W/nf * 0.29' as='int((nf+2)/2) * W/nf * 0.29'
+ pd='2*int((nf+1)/2) * (W/nf + 0.29)' ps='2*int((nf+2)/2) * (W/nf + 0.29)' nrd='0.29 / W' nrs='0.29 / W'
+ sa=0 sb=0 sd=0 mult=1 m=1
XM5 net6 net1 GND GND sky130_fd_pr__nfet_01v8 L=4 W=0.55 nf=1 ad='int((nf+1)/2) * W/nf * 0.29' as='int((nf+2)/2) * W/nf * 0.29'
+ pd='2*int((nf+1)/2) * (W/nf + 0.29)' ps='2*int((nf+2)/2) * (W/nf + 0.29)' nrd='0.29 / W' nrs='0.29 / W'
+ sa=0 sb=0 sd=0 mult=1 m=1
XM6 net3 vctrl net4 net4 sky130_fd_pr__pfet_01v8 L=2 W=1 nf=1 ad='int((nf+1)/2) * W/nf * 0.29' as='int((nf+2)/2) * W/nf * 0.29'
+ pd='2*int((nf+1)/2) * (W/nf + 0.29)' ps='2*int((nf+2)/2) * (W/nf + 0.29)' nrd='0.29 / W' nrs='0.29 / W'
+ sa=0 sb=0 sd=0 mult=1 m=1
XM7 net7 net5 net8 GND sky130_fd_pr__nfet_01v8 L=4 W=0.55 nf=1 ad='int((nf+1)/2) * W/nf * 0.29' as='int((nf+2)/2) * W/nf * 0.29'
+ pd='2*int((nf+1)/2) * (W/nf + 0.29)' ps='2*int((nf+2)/2) * (W/nf + 0.29)' nrd='0.29 / W' nrs='0.29 / W'
+ sa=0 sb=0 sd=0 mult=1 m=1
XM8 net7 net5 net3 net4 sky130_fd_pr__pfet_01v8 L=4 W=1 nf=1 ad='int((nf+1)/2) * W/nf * 0.29' as='int((nf+2)/2) * W/nf * 0.29'
+ pd='2*int((nf+1)/2) * (W/nf + 0.29)' ps='2*int((nf+2)/2) * (W/nf + 0.29)' nrd='0.29 / W' nrs='0.29 / W'
+ sa=0 sb=0 sd=0 mult=1 m=1
XM9 net8 net5 GND GND sky130_fd_pr__nfet_01v8 L=4 W=0.55 nf=1 ad='int((nf+1)/2) * W/nf * 0.29' as='int((nf+2)/2) * W/nf * 0.29'
+ pd='2*int((nf+1)/2) * (W/nf + 0.29)' ps='2*int((nf+2)/2) * (W/nf + 0.29)' nrd='0.29 / W' nrs='0.29 / W'
+ sa=0 sb=0 sd=0 mult=1 m=1
XM10 net3 vctrl net4 net4 sky130_fd_pr__pfet_01v8 L=2 W=1 nf=1 ad='int((nf+1)/2) * W/nf * 0.29' as='int((nf+2)/2) * W/nf * 0.29'
+ pd='2*int((nf+1)/2) * (W/nf + 0.29)' ps='2*int((nf+2)/2) * (W/nf + 0.29)' nrd='0.29 / W' nrs='0.29 / W'
+ sa=0 sb=0 sd=0 mult=1 m=1
XM11 net9 net7 net10 GND sky130_fd_pr__nfet_01v8 L=4 W=0.55 nf=1 ad='int((nf+1)/2) * W/nf * 0.29' as='int((nf+2)/2) * W/nf * 0.29'
+ pd='2*int((nf+1)/2) * (W/nf + 0.29)' ps='2*int((nf+2)/2) * (W/nf + 0.29)' nrd='0.29 / W' nrs='0.29 / W'
+ sa=0 sb=0 sd=0 mult=1 m=1
XM12 net9 net7 net3 net4 sky130_fd_pr__pfet_01v8 L=4 W=1 nf=1 ad='int((nf+1)/2) * W/nf * 0.29' as='int((nf+2)/2) * W/nf * 0.29'
+ pd='2*int((nf+1)/2) * (W/nf + 0.29)' ps='2*int((nf+2)/2) * (W/nf + 0.29)' nrd='0.29 / W' nrs='0.29 / W'
+ sa=0 sb=0 sd=0 mult=1 m=1
XM13 net10 net7 GND GND sky130_fd_pr__nfet_01v8 L=4 W=0.55 nf=1 ad='int((nf+1)/2) * W/nf * 0.29' as='int((nf+2)/2) * W/nf * 0.29'
+ pd='2*int((nf+1)/2) * (W/nf + 0.29)' ps='2*int((nf+2)/2) * (W/nf + 0.29)' nrd='0.29 / W' nrs='0.29 / W'
+ sa=0 sb=0 sd=0 mult=1 m=1
XM14 net3 vctrl net4 net4 sky130_fd_pr__pfet_01v8 L=2 W=1 nf=1 ad='int((nf+1)/2) * W/nf * 0.29' as='int((nf+2)/2) * W/nf * 0.29'
+ pd='2*int((nf+1)/2) * (W/nf + 0.29)' ps='2*int((nf+2)/2) * (W/nf + 0.29)' nrd='0.29 / W' nrs='0.29 / W'
+ sa=0 sb=0 sd=0 mult=1 m=1
XM15 net11 net9 net12 GND sky130_fd_pr__nfet_01v8 L=4 W=0.55 nf=1 ad='int((nf+1)/2) * W/nf * 0.29' as='int((nf+2)/2) * W/nf * 0.29'
+ pd='2*int((nf+1)/2) * (W/nf + 0.29)' ps='2*int((nf+2)/2) * (W/nf + 0.29)' nrd='0.29 / W' nrs='0.29 / W'
+ sa=0 sb=0 sd=0 mult=1 m=1
XM16 net11 net9 net3 net4 sky130_fd_pr__pfet_01v8 L=4 W=1 nf=1 ad='int((nf+1)/2) * W/nf * 0.29' as='int((nf+2)/2) * W/nf * 0.29'
+ pd='2*int((nf+1)/2) * (W/nf + 0.29)' ps='2*int((nf+2)/2) * (W/nf + 0.29)' nrd='0.29 / W' nrs='0.29 / W'
+ sa=0 sb=0 sd=0 mult=1 m=1
XM17 net12 net9 GND GND sky130_fd_pr__nfet_01v8 L=4 W=0.55 nf=1 ad='int((nf+1)/2) * W/nf * 0.29' as='int((nf+2)/2) * W/nf * 0.29'
+ pd='2*int((nf+1)/2) * (W/nf + 0.29)' ps='2*int((nf+2)/2) * (W/nf + 0.29)' nrd='0.29 / W' nrs='0.29 / W'
+ sa=0 sb=0 sd=0 mult=1 m=1
XM18 net3 vctrl net4 net4 sky130_fd_pr__pfet_01v8 L=2 W=1 nf=1 ad='int((nf+1)/2) * W/nf * 0.29' as='int((nf+2)/2) * W/nf * 0.29'
+ pd='2*int((nf+1)/2) * (W/nf + 0.29)' ps='2*int((nf+2)/2) * (W/nf + 0.29)' nrd='0.29 / W' nrs='0.29 / W'
+ sa=0 sb=0 sd=0 mult=1 m=1
XM20 net13 net11 net14 GND sky130_fd_pr__nfet_01v8 L=4 W=0.55 nf=1 ad='int((nf+1)/2) * W/nf * 0.29' as='int((nf+2)/2) * W/nf * 0.29'
+ pd='2*int((nf+1)/2) * (W/nf + 0.29)' ps='2*int((nf+2)/2) * (W/nf + 0.29)' nrd='0.29 / W' nrs='0.29 / W'
+ sa=0 sb=0 sd=0 mult=1 m=1
XM21 net13 net11 net3 net4 sky130_fd_pr__pfet_01v8 L=4 W=1 nf=1 ad='int((nf+1)/2) * W/nf * 0.29' as='int((nf+2)/2) * W/nf * 0.29'
+ pd='2*int((nf+1)/2) * (W/nf + 0.29)' ps='2*int((nf+2)/2) * (W/nf + 0.29)' nrd='0.29 / W' nrs='0.29 / W'
+ sa=0 sb=0 sd=0 mult=1 m=1
XM22 net14 net11 GND GND sky130_fd_pr__nfet_01v8 L=4 W=0.55 nf=1 ad='int((nf+1)/2) * W/nf * 0.29' as='int((nf+2)/2) * W/nf * 0.29'
+ pd='2*int((nf+1)/2) * (W/nf + 0.29)' ps='2*int((nf+2)/2) * (W/nf + 0.29)' nrd='0.29 / W' nrs='0.29 / W'
+ sa=0 sb=0 sd=0 mult=1 m=1
XM23 net3 vctrl net4 net4 sky130_fd_pr__pfet_01v8 L=2 W=1 nf=1 ad='int((nf+1)/2) * W/nf * 0.29' as='int((nf+2)/2) * W/nf * 0.29'
+ pd='2*int((nf+1)/2) * (W/nf + 0.29)' ps='2*int((nf+2)/2) * (W/nf + 0.29)' nrd='0.29 / W' nrs='0.29 / W'
+ sa=0 sb=0 sd=0 mult=1 m=1
XM24 net15 net13 net16 GND sky130_fd_pr__nfet_01v8 L=4 W=0.55 nf=1 ad='int((nf+1)/2) * W/nf * 0.29' as='int((nf+2)/2) * W/nf * 0.29'
+ pd='2*int((nf+1)/2) * (W/nf + 0.29)' ps='2*int((nf+2)/2) * (W/nf + 0.29)' nrd='0.29 / W' nrs='0.29 / W'
+ sa=0 sb=0 sd=0 mult=1 m=1
XM25 net15 net13 net3 net4 sky130_fd_pr__pfet_01v8 L=4 W=1 nf=1 ad='int((nf+1)/2) * W/nf * 0.29' as='int((nf+2)/2) * W/nf * 0.29'
+ pd='2*int((nf+1)/2) * (W/nf + 0.29)' ps='2*int((nf+2)/2) * (W/nf + 0.29)' nrd='0.29 / W' nrs='0.29 / W'
+ sa=0 sb=0 sd=0 mult=1 m=1
XM26 net16 net13 GND GND sky130_fd_pr__nfet_01v8 L=4 W=0.55 nf=1 ad='int((nf+1)/2) * W/nf * 0.29' as='int((nf+2)/2) * W/nf * 0.29'
+ pd='2*int((nf+1)/2) * (W/nf + 0.29)' ps='2*int((nf+2)/2) * (W/nf + 0.29)' nrd='0.29 / W' nrs='0.29 / W'
+ sa=0 sb=0 sd=0 mult=1 m=1
XM27 net3 vctrl net4 net4 sky130_fd_pr__pfet_01v8 L=2 W=1 nf=1 ad='int((nf+1)/2) * W/nf * 0.29' as='int((nf+2)/2) * W/nf * 0.29'
+ pd='2*int((nf+1)/2) * (W/nf + 0.29)' ps='2*int((nf+2)/2) * (W/nf + 0.29)' nrd='0.29 / W' nrs='0.29 / W'
+ sa=0 sb=0 sd=0 mult=1 m=1
XM28 net17 net15 net18 GND sky130_fd_pr__nfet_01v8 L=4 W=0.55 nf=1 ad='int((nf+1)/2) * W/nf * 0.29' as='int((nf+2)/2) * W/nf * 0.29'
+ pd='2*int((nf+1)/2) * (W/nf + 0.29)' ps='2*int((nf+2)/2) * (W/nf + 0.29)' nrd='0.29 / W' nrs='0.29 / W'
+ sa=0 sb=0 sd=0 mult=1 m=1
XM30 net17 net15 net3 net4 sky130_fd_pr__pfet_01v8 L=4 W=1 nf=1 ad='int((nf+1)/2) * W/nf * 0.29' as='int((nf+2)/2) * W/nf * 0.29'
+ pd='2*int((nf+1)/2) * (W/nf + 0.29)' ps='2*int((nf+2)/2) * (W/nf + 0.29)' nrd='0.29 / W' nrs='0.29 / W'
+ sa=0 sb=0 sd=0 mult=1 m=1
XM31 net18 net15 GND GND sky130_fd_pr__nfet_01v8 L=4 W=0.55 nf=1 ad='int((nf+1)/2) * W/nf * 0.29' as='int((nf+2)/2) * W/nf * 0.29'
+ pd='2*int((nf+1)/2) * (W/nf + 0.29)' ps='2*int((nf+2)/2) * (W/nf + 0.29)' nrd='0.29 / W' nrs='0.29 / W'
+ sa=0 sb=0 sd=0 mult=1 m=1
XM32 net3 vctrl net4 net4 sky130_fd_pr__pfet_01v8 L=2 W=1 nf=1 ad='int((nf+1)/2) * W/nf * 0.29' as='int((nf+2)/2) * W/nf * 0.29'
+ pd='2*int((nf+1)/2) * (W/nf + 0.29)' ps='2*int((nf+2)/2) * (W/nf + 0.29)' nrd='0.29 / W' nrs='0.29 / W'
+ sa=0 sb=0 sd=0 mult=1 m=1
XM33 vout net17 net19 GND sky130_fd_pr__nfet_01v8 L=4 W=0.55 nf=1 ad='int((nf+1)/2) * W/nf * 0.29' as='int((nf+2)/2) * W/nf * 0.29'
+ pd='2*int((nf+1)/2) * (W/nf + 0.29)' ps='2*int((nf+2)/2) * (W/nf + 0.29)' nrd='0.29 / W' nrs='0.29 / W'
+ sa=0 sb=0 sd=0 mult=1 m=1
XM34 vout net17 net3 net4 sky130_fd_pr__pfet_01v8 L=4 W=1 nf=1 ad='int((nf+1)/2) * W/nf * 0.29' as='int((nf+2)/2) * W/nf * 0.29'
+ pd='2*int((nf+1)/2) * (W/nf + 0.29)' ps='2*int((nf+2)/2) * (W/nf + 0.29)' nrd='0.29 / W' nrs='0.29 / W'
+ sa=0 sb=0 sd=0 mult=1 m=1
XM35 net19 net17 GND GND sky130_fd_pr__nfet_01v8 L=4 W=0.55 nf=1 ad='int((nf+1)/2) * W/nf * 0.29' as='int((nf+2)/2) * W/nf * 0.29'
+ pd='2*int((nf+1)/2) * (W/nf + 0.29)' ps='2*int((nf+2)/2) * (W/nf + 0.29)' nrd='0.29 / W' nrs='0.29 / W'
+ sa=0 sb=0 sd=0 mult=1 m=1
XM36 net3 vctrl net4 net4 sky130_fd_pr__pfet_01v8 L=2 W=1 nf=1 ad='int((nf+1)/2) * W/nf * 0.29' as='int((nf+2)/2) * W/nf * 0.29'
+ pd='2*int((nf+1)/2) * (W/nf + 0.29)' ps='2*int((nf+2)/2) * (W/nf + 0.29)' nrd='0.29 / W' nrs='0.29 / W'
+ sa=0 sb=0 sd=0 mult=1 m=1
.ends

.GLOBAL GND
.end
